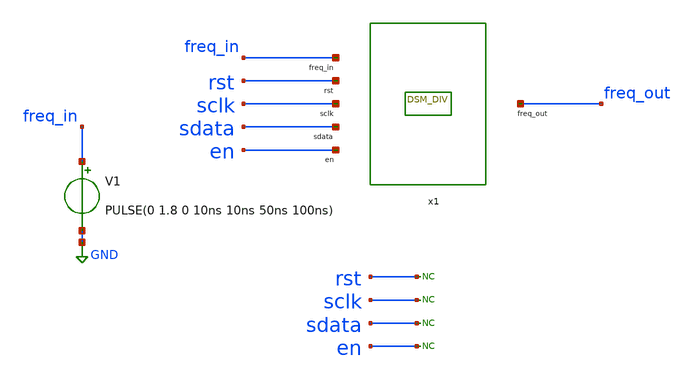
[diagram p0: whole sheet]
** sch_path: schematic/dsm/xschem/dsm_with_mdiv_pex_tb.sch
* Copyright (C) 1998-2024 Stefan Frederik Schippers
* This program is free software; you can redistribute it and/or modify
* it under the terms of the GNU General Public License as published by
* the Free Software Foundation; either version 2 of the License, or
* (at your option) any later version.
* This program is distributed in the hope that it will be useful,
* but WITHOUT ANY WARRANTY; without even the implied warranty of
* MERCHANTABILITY or FITNESS FOR A PARTICULAR PURPOSE.  See the
* GNU General Public License for more details.
* You should have received a copy of the GNU General Public License
* along with this program; if not, write to the Free Software
**.subckt dsm_with_mdiv_pex_tb
V1 freq_in GND PULSE(0 1.8 0 10ns 10ns 50ns 100ns)
* noconn rst
* noconn sclk
* noconn sdata
* noconn en
x1 freq_in rst sclk sdata en freq_out dsm_and_freq_divider_pex
**** begin user architecture code



.include ./dsm_and_freq_divider.pex.spice
* ngspice commands
.save v(dout) v(sdata) v(sclk) v(en) v(rst) v(dsm_clk) v(freq_in) v(freq_out)
.control
  tran 0.5n 1m
  remzerovec
  write test.raw
.endc

* to generate following file copy stimuli.test
* to the simulation directory and run simulation -> Utile Stimuli Editor (GUI),
* and press 'Translate'
.include stimuli_test.cir



**** end user architecture code
**.ends
.GLOBAL GND
.end
